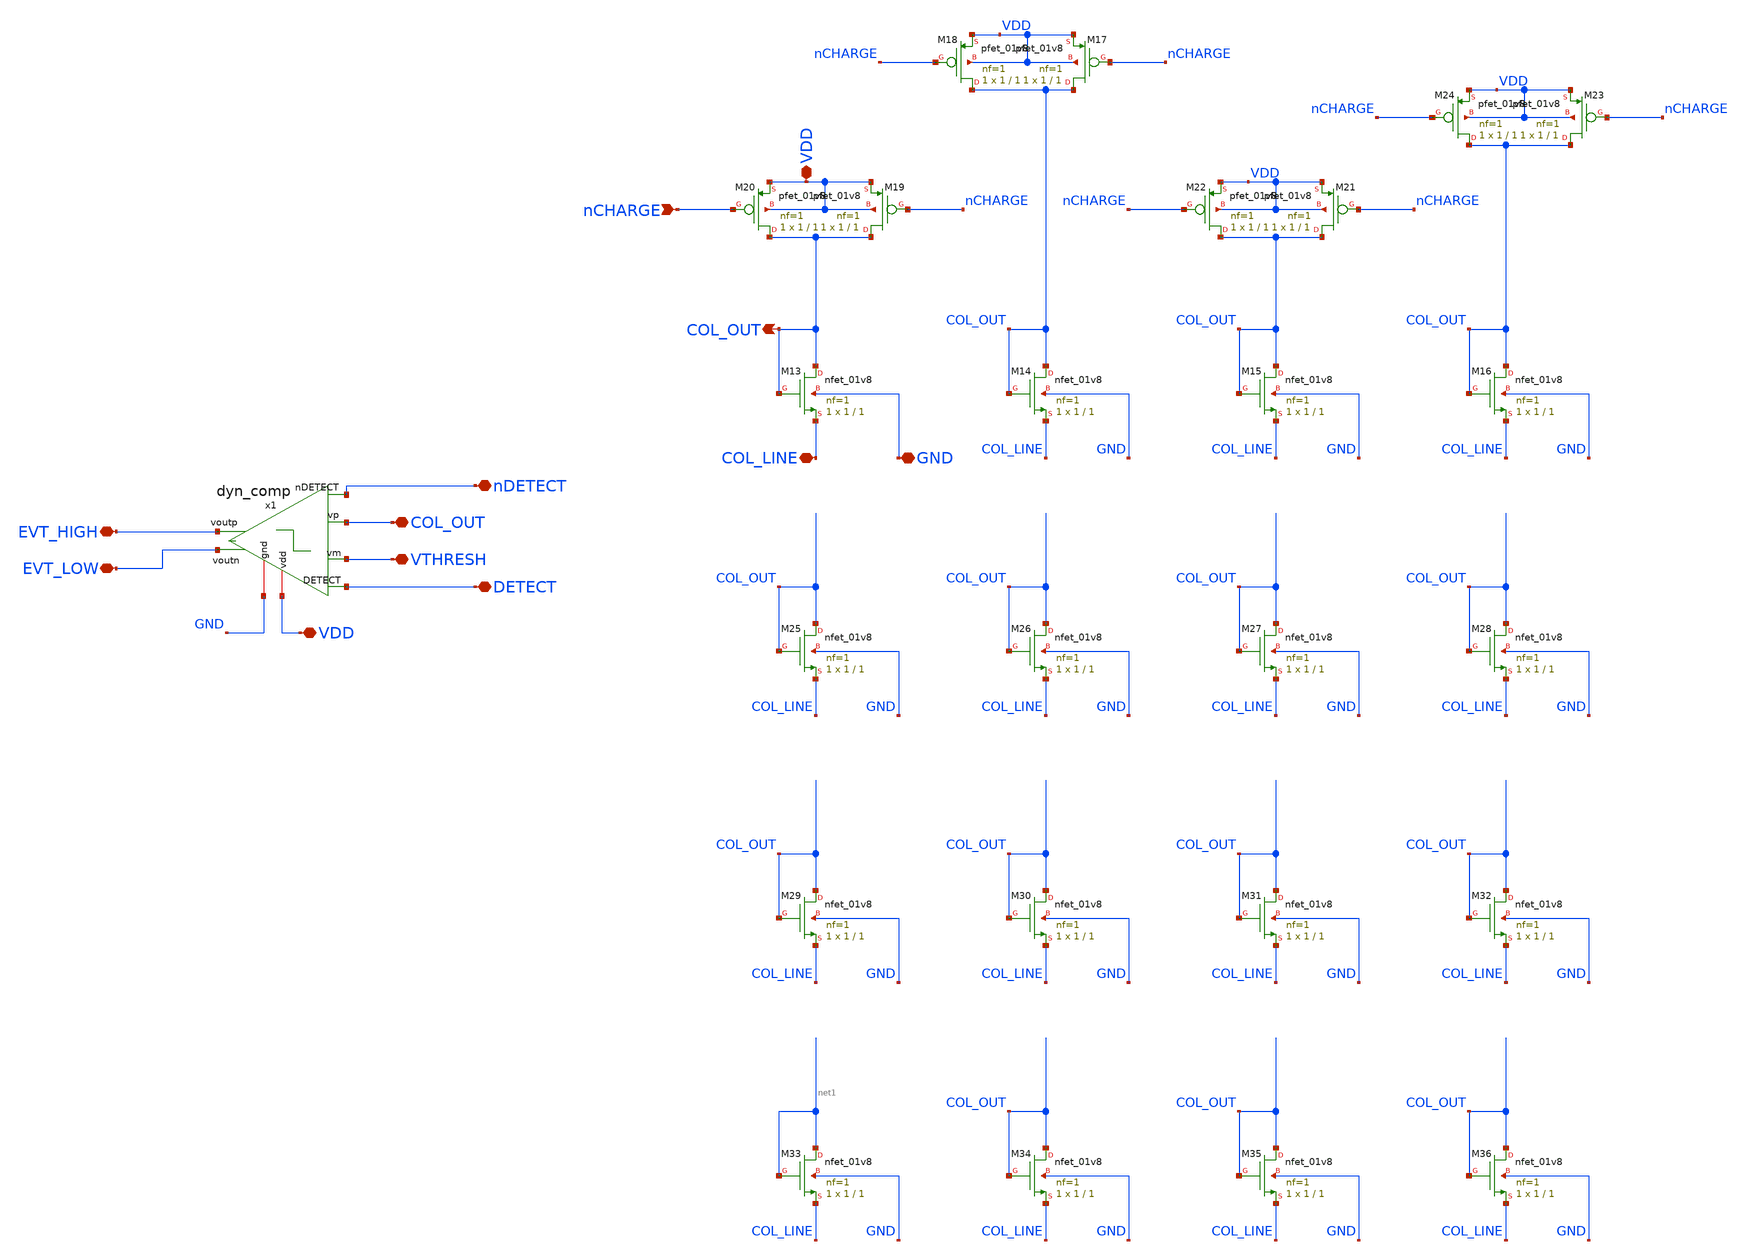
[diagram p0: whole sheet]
** sch_path: analog/xschem/col_amp_v2_std_vds/xschem/column_gds.sch
**.subckt column_gds DETECT VTHRESH VDD EVT_HIGH EVT_LOW nDETECT COL_OUT nCHARGE COL_OUT VDD GND
*+ COL_LINE
*.iopin DETECT
*.iopin VTHRESH
*.iopin VDD
*.iopin EVT_HIGH
*.iopin EVT_LOW
*.iopin nDETECT
*.iopin COL_OUT
*.ipin nCHARGE
*.opin COL_OUT
*.iopin VDD
*.iopin GND
*.iopin COL_LINE
XM13 COL_OUT COL_OUT COL_LINE GND sky130_fd_pr__nfet_01v8 L=1 W=1 nf=1 ad='int((1 + 1)/2) * 1 / 1 * 0.29'
+ as='int((1 + 2)/2) * 1 / 1 * 0.29' pd='2*int((1 + 1)/2) * (1 / 1 + 0.29)' ps='2*int((1 + 2)/2) * (1 / 1 + 0.29)'
+ nrd='0.29 / 1 ' nrs='0.29 / 1 ' sa=0 sb=0 sd=0 mult=1 m=1
XM14 COL_OUT COL_OUT COL_LINE GND sky130_fd_pr__nfet_01v8 L=1 W=1 nf=1 ad='int((1 + 1)/2) * 1 / 1 * 0.29'
+ as='int((1 + 2)/2) * 1 / 1 * 0.29' pd='2*int((1 + 1)/2) * (1 / 1 + 0.29)' ps='2*int((1 + 2)/2) * (1 / 1 + 0.29)'
+ nrd='0.29 / 1 ' nrs='0.29 / 1 ' sa=0 sb=0 sd=0 mult=1 m=1
XM15 COL_OUT COL_OUT COL_LINE GND sky130_fd_pr__nfet_01v8 L=1 W=1 nf=1 ad='int((1 + 1)/2) * 1 / 1 * 0.29'
+ as='int((1 + 2)/2) * 1 / 1 * 0.29' pd='2*int((1 + 1)/2) * (1 / 1 + 0.29)' ps='2*int((1 + 2)/2) * (1 / 1 + 0.29)'
+ nrd='0.29 / 1 ' nrs='0.29 / 1 ' sa=0 sb=0 sd=0 mult=1 m=1
XM16 COL_OUT COL_OUT COL_LINE GND sky130_fd_pr__nfet_01v8 L=1 W=1 nf=1 ad='int((1 + 1)/2) * 1 / 1 * 0.29'
+ as='int((1 + 2)/2) * 1 / 1 * 0.29' pd='2*int((1 + 1)/2) * (1 / 1 + 0.29)' ps='2*int((1 + 2)/2) * (1 / 1 + 0.29)'
+ nrd='0.29 / 1 ' nrs='0.29 / 1 ' sa=0 sb=0 sd=0 mult=1 m=1
XM17 COL_OUT nCHARGE VDD VDD sky130_fd_pr__pfet_01v8 L=1 W=1 nf=1 ad='int((1 + 1)/2) * 1 / 1 * 0.29'
+ as='int((1 + 2)/2) * 1 / 1 * 0.29' pd='2*int((1 + 1)/2) * (1 / 1 + 0.29)' ps='2*int((1 + 2)/2) * (1 / 1 + 0.29)'
+ nrd='0.29 / 1 ' nrs='0.29 / 1 ' sa=0 sb=0 sd=0 mult=1 m=1
XM18 COL_OUT nCHARGE VDD VDD sky130_fd_pr__pfet_01v8 L=1 W=1 nf=1 ad='int((1 + 1)/2) * 1 / 1 * 0.29'
+ as='int((1 + 2)/2) * 1 / 1 * 0.29' pd='2*int((1 + 1)/2) * (1 / 1 + 0.29)' ps='2*int((1 + 2)/2) * (1 / 1 + 0.29)'
+ nrd='0.29 / 1 ' nrs='0.29 / 1 ' sa=0 sb=0 sd=0 mult=1 m=1
XM19 COL_OUT nCHARGE VDD VDD sky130_fd_pr__pfet_01v8 L=1 W=1 nf=1 ad='int((1 + 1)/2) * 1 / 1 * 0.29'
+ as='int((1 + 2)/2) * 1 / 1 * 0.29' pd='2*int((1 + 1)/2) * (1 / 1 + 0.29)' ps='2*int((1 + 2)/2) * (1 / 1 + 0.29)'
+ nrd='0.29 / 1 ' nrs='0.29 / 1 ' sa=0 sb=0 sd=0 mult=1 m=1
XM20 COL_OUT nCHARGE VDD VDD sky130_fd_pr__pfet_01v8 L=1 W=1 nf=1 ad='int((1 + 1)/2) * 1 / 1 * 0.29'
+ as='int((1 + 2)/2) * 1 / 1 * 0.29' pd='2*int((1 + 1)/2) * (1 / 1 + 0.29)' ps='2*int((1 + 2)/2) * (1 / 1 + 0.29)'
+ nrd='0.29 / 1 ' nrs='0.29 / 1 ' sa=0 sb=0 sd=0 mult=1 m=1
XM21 COL_OUT nCHARGE VDD VDD sky130_fd_pr__pfet_01v8 L=1 W=1 nf=1 ad='int((1 + 1)/2) * 1 / 1 * 0.29'
+ as='int((1 + 2)/2) * 1 / 1 * 0.29' pd='2*int((1 + 1)/2) * (1 / 1 + 0.29)' ps='2*int((1 + 2)/2) * (1 / 1 + 0.29)'
+ nrd='0.29 / 1 ' nrs='0.29 / 1 ' sa=0 sb=0 sd=0 mult=1 m=1
XM22 COL_OUT nCHARGE VDD VDD sky130_fd_pr__pfet_01v8 L=1 W=1 nf=1 ad='int((1 + 1)/2) * 1 / 1 * 0.29'
+ as='int((1 + 2)/2) * 1 / 1 * 0.29' pd='2*int((1 + 1)/2) * (1 / 1 + 0.29)' ps='2*int((1 + 2)/2) * (1 / 1 + 0.29)'
+ nrd='0.29 / 1 ' nrs='0.29 / 1 ' sa=0 sb=0 sd=0 mult=1 m=1
XM23 COL_OUT nCHARGE VDD VDD sky130_fd_pr__pfet_01v8 L=1 W=1 nf=1 ad='int((1 + 1)/2) * 1 / 1 * 0.29'
+ as='int((1 + 2)/2) * 1 / 1 * 0.29' pd='2*int((1 + 1)/2) * (1 / 1 + 0.29)' ps='2*int((1 + 2)/2) * (1 / 1 + 0.29)'
+ nrd='0.29 / 1 ' nrs='0.29 / 1 ' sa=0 sb=0 sd=0 mult=1 m=1
XM24 COL_OUT nCHARGE VDD VDD sky130_fd_pr__pfet_01v8 L=1 W=1 nf=1 ad='int((1 + 1)/2) * 1 / 1 * 0.29'
+ as='int((1 + 2)/2) * 1 / 1 * 0.29' pd='2*int((1 + 1)/2) * (1 / 1 + 0.29)' ps='2*int((1 + 2)/2) * (1 / 1 + 0.29)'
+ nrd='0.29 / 1 ' nrs='0.29 / 1 ' sa=0 sb=0 sd=0 mult=1 m=1
XM25 COL_OUT COL_OUT COL_LINE GND sky130_fd_pr__nfet_01v8 L=1 W=1 nf=1 ad='int((1 + 1)/2) * 1 / 1 * 0.29'
+ as='int((1 + 2)/2) * 1 / 1 * 0.29' pd='2*int((1 + 1)/2) * (1 / 1 + 0.29)' ps='2*int((1 + 2)/2) * (1 / 1 + 0.29)'
+ nrd='0.29 / 1 ' nrs='0.29 / 1 ' sa=0 sb=0 sd=0 mult=1 m=1
XM26 COL_OUT COL_OUT COL_LINE GND sky130_fd_pr__nfet_01v8 L=1 W=1 nf=1 ad='int((1 + 1)/2) * 1 / 1 * 0.29'
+ as='int((1 + 2)/2) * 1 / 1 * 0.29' pd='2*int((1 + 1)/2) * (1 / 1 + 0.29)' ps='2*int((1 + 2)/2) * (1 / 1 + 0.29)'
+ nrd='0.29 / 1 ' nrs='0.29 / 1 ' sa=0 sb=0 sd=0 mult=1 m=1
XM27 COL_OUT COL_OUT COL_LINE GND sky130_fd_pr__nfet_01v8 L=1 W=1 nf=1 ad='int((1 + 1)/2) * 1 / 1 * 0.29'
+ as='int((1 + 2)/2) * 1 / 1 * 0.29' pd='2*int((1 + 1)/2) * (1 / 1 + 0.29)' ps='2*int((1 + 2)/2) * (1 / 1 + 0.29)'
+ nrd='0.29 / 1 ' nrs='0.29 / 1 ' sa=0 sb=0 sd=0 mult=1 m=1
XM28 COL_OUT COL_OUT COL_LINE GND sky130_fd_pr__nfet_01v8 L=1 W=1 nf=1 ad='int((1 + 1)/2) * 1 / 1 * 0.29'
+ as='int((1 + 2)/2) * 1 / 1 * 0.29' pd='2*int((1 + 1)/2) * (1 / 1 + 0.29)' ps='2*int((1 + 2)/2) * (1 / 1 + 0.29)'
+ nrd='0.29 / 1 ' nrs='0.29 / 1 ' sa=0 sb=0 sd=0 mult=1 m=1
XM29 COL_OUT COL_OUT COL_LINE GND sky130_fd_pr__nfet_01v8 L=1 W=1 nf=1 ad='int((1 + 1)/2) * 1 / 1 * 0.29'
+ as='int((1 + 2)/2) * 1 / 1 * 0.29' pd='2*int((1 + 1)/2) * (1 / 1 + 0.29)' ps='2*int((1 + 2)/2) * (1 / 1 + 0.29)'
+ nrd='0.29 / 1 ' nrs='0.29 / 1 ' sa=0 sb=0 sd=0 mult=1 m=1
XM30 COL_OUT COL_OUT COL_LINE GND sky130_fd_pr__nfet_01v8 L=1 W=1 nf=1 ad='int((1 + 1)/2) * 1 / 1 * 0.29'
+ as='int((1 + 2)/2) * 1 / 1 * 0.29' pd='2*int((1 + 1)/2) * (1 / 1 + 0.29)' ps='2*int((1 + 2)/2) * (1 / 1 + 0.29)'
+ nrd='0.29 / 1 ' nrs='0.29 / 1 ' sa=0 sb=0 sd=0 mult=1 m=1
XM31 COL_OUT COL_OUT COL_LINE GND sky130_fd_pr__nfet_01v8 L=1 W=1 nf=1 ad='int((1 + 1)/2) * 1 / 1 * 0.29'
+ as='int((1 + 2)/2) * 1 / 1 * 0.29' pd='2*int((1 + 1)/2) * (1 / 1 + 0.29)' ps='2*int((1 + 2)/2) * (1 / 1 + 0.29)'
+ nrd='0.29 / 1 ' nrs='0.29 / 1 ' sa=0 sb=0 sd=0 mult=1 m=1
XM32 COL_OUT COL_OUT COL_LINE GND sky130_fd_pr__nfet_01v8 L=1 W=1 nf=1 ad='int((1 + 1)/2) * 1 / 1 * 0.29'
+ as='int((1 + 2)/2) * 1 / 1 * 0.29' pd='2*int((1 + 1)/2) * (1 / 1 + 0.29)' ps='2*int((1 + 2)/2) * (1 / 1 + 0.29)'
+ nrd='0.29 / 1 ' nrs='0.29 / 1 ' sa=0 sb=0 sd=0 mult=1 m=1
XM33 net1 net1 COL_LINE GND sky130_fd_pr__nfet_01v8 L=1 W=1 nf=1 ad='int((1 + 1)/2) * 1 / 1 * 0.29' as='int((1 + 2)/2) * 1 / 1 * 0.29'
+ pd='2*int((1 + 1)/2) * (1 / 1 + 0.29)' ps='2*int((1 + 2)/2) * (1 / 1 + 0.29)' nrd='0.29 / 1 ' nrs='0.29 / 1 '
+ sa=0 sb=0 sd=0 mult=1 m=1
XM34 COL_OUT COL_OUT COL_LINE GND sky130_fd_pr__nfet_01v8 L=1 W=1 nf=1 ad='int((1 + 1)/2) * 1 / 1 * 0.29'
+ as='int((1 + 2)/2) * 1 / 1 * 0.29' pd='2*int((1 + 1)/2) * (1 / 1 + 0.29)' ps='2*int((1 + 2)/2) * (1 / 1 + 0.29)'
+ nrd='0.29 / 1 ' nrs='0.29 / 1 ' sa=0 sb=0 sd=0 mult=1 m=1
XM35 COL_OUT COL_OUT COL_LINE GND sky130_fd_pr__nfet_01v8 L=1 W=1 nf=1 ad='int((1 + 1)/2) * 1 / 1 * 0.29'
+ as='int((1 + 2)/2) * 1 / 1 * 0.29' pd='2*int((1 + 1)/2) * (1 / 1 + 0.29)' ps='2*int((1 + 2)/2) * (1 / 1 + 0.29)'
+ nrd='0.29 / 1 ' nrs='0.29 / 1 ' sa=0 sb=0 sd=0 mult=1 m=1
XM36 COL_OUT COL_OUT COL_LINE GND sky130_fd_pr__nfet_01v8 L=1 W=1 nf=1 ad='int((1 + 1)/2) * 1 / 1 * 0.29'
+ as='int((1 + 2)/2) * 1 / 1 * 0.29' pd='2*int((1 + 1)/2) * (1 / 1 + 0.29)' ps='2*int((1 + 2)/2) * (1 / 1 + 0.29)'
+ nrd='0.29 / 1 ' nrs='0.29 / 1 ' sa=0 sb=0 sd=0 mult=1 m=1
x1 VDD COL_OUT VTHRESH GND nDETECT DETECT EVT_HIGH EVT_LOW dyn_comp
**.ends

* expanding   symbol:  dyn_comp.sym # of pins=8
** sym_path: analog/xschem/col_amp_v2_std_dvs/xschem/dyn_comp.sym
** sch_path: analog/xschem/col_amp_v2_std_dvs/xschem/dyn_comp.sch
.subckt dyn_comp vdd vp vm gnd nDETECT DETECT voutp voutn
*.iopin vdd
*.iopin gnd
*.ipin vp
*.ipin vm
*.ipin nDETECT
*.opin voutn
*.opin voutp
*.ipin DETECT
XMmirr3 int_outn DETECT vdd vdd sky130_fd_pr__pfet_01v8 L=0.5 W=1 nf=1 ad='int((1 + 1)/2) * 1 / 1 * 0.29'
+ as='int((1 + 2)/2) * 1 / 1 * 0.29' pd='2*int((1 + 1)/2) * (1 / 1 + 0.29)' ps='2*int((1 + 2)/2) * (1 / 1 + 0.29)'
+ nrd='0.29 / 1 ' nrs='0.29 / 1 ' sa=0 sb=0 sd=0 mult=1 m=1
XMdio2 int_outp DETECT vdd vdd sky130_fd_pr__pfet_01v8 L=0.5 W=1 nf=1 ad='int((1 + 1)/2) * 1 / 1 * 0.29'
+ as='int((1 + 2)/2) * 1 / 1 * 0.29' pd='2*int((1 + 1)/2) * (1 / 1 + 0.29)' ps='2*int((1 + 2)/2) * (1 / 1 + 0.29)'
+ nrd='0.29 / 1 ' nrs='0.29 / 1 ' sa=0 sb=0 sd=0 mult=1 m=1
XMinm3 int_outp vp vsource gnd sky130_fd_pr__nfet_01v8 L=0.15 W=1 nf=1 ad='int((1 + 1)/2) * 1 / 1 * 0.29'
+ as='int((1 + 2)/2) * 1 / 1 * 0.29' pd='2*int((1 + 1)/2) * (1 / 1 + 0.29)' ps='2*int((1 + 2)/2) * (1 / 1 + 0.29)'
+ nrd='0.29 / 1 ' nrs='0.29 / 1 ' sa=0 sb=0 sd=0 mult=1 m=1
XMinp3 int_outn vm vsource gnd sky130_fd_pr__nfet_01v8 L=0.15 W=1 nf=1 ad='int((1 + 1)/2) * 1 / 1 * 0.29'
+ as='int((1 + 2)/2) * 1 / 1 * 0.29' pd='2*int((1 + 1)/2) * (1 / 1 + 0.29)' ps='2*int((1 + 2)/2) * (1 / 1 + 0.29)'
+ nrd='0.29 / 1 ' nrs='0.29 / 1 ' sa=0 sb=0 sd=0 mult=1 m=1
XMbias1 vsource DETECT gnd gnd sky130_fd_pr__nfet_01v8 L=0.15 W=1 nf=1 ad='int((1 + 1)/2) * 1 / 1 * 0.29'
+ as='int((1 + 2)/2) * 1 / 1 * 0.29' pd='2*int((1 + 1)/2) * (1 / 1 + 0.29)' ps='2*int((1 + 2)/2) * (1 / 1 + 0.29)'
+ nrd='0.29 / 1 ' nrs='0.29 / 1 ' sa=0 sb=0 sd=0 mult=1 m=1
XMmirr4 net3 nDETECT vdd vdd sky130_fd_pr__pfet_01v8 L=0.5 W=1 nf=1 ad='int((1 + 1)/2) * 1 / 1 * 0.29'
+ as='int((1 + 2)/2) * 1 / 1 * 0.29' pd='2*int((1 + 1)/2) * (1 / 1 + 0.29)' ps='2*int((1 + 2)/2) * (1 / 1 + 0.29)'
+ nrd='0.29 / 1 ' nrs='0.29 / 1 ' sa=0 sb=0 sd=0 mult=1 m=1
XMmirr5 net2 net1 net3 vdd sky130_fd_pr__pfet_01v8 L=0.5 W=1 nf=1 ad='int((1 + 1)/2) * 1 / 1 * 0.29'
+ as='int((1 + 2)/2) * 1 / 1 * 0.29' pd='2*int((1 + 1)/2) * (1 / 1 + 0.29)' ps='2*int((1 + 2)/2) * (1 / 1 + 0.29)'
+ nrd='0.29 / 1 ' nrs='0.29 / 1 ' sa=0 sb=0 sd=0 mult=1 m=1
XMdio3 net1 net2 net3 vdd sky130_fd_pr__pfet_01v8 L=0.5 W=1 nf=1 ad='int((1 + 1)/2) * 1 / 1 * 0.29' as='int((1 + 2)/2) * 1 / 1 * 0.29'
+ pd='2*int((1 + 1)/2) * (1 / 1 + 0.29)' ps='2*int((1 + 2)/2) * (1 / 1 + 0.29)' nrd='0.29 / 1 ' nrs='0.29 / 1 '
+ sa=0 sb=0 sd=0 mult=1 m=1
XMinp4 net1 net2 gnd gnd sky130_fd_pr__nfet_01v8 L=0.15 W=1 nf=1 ad='int((1 + 1)/2) * 1 / 1 * 0.29' as='int((1 + 2)/2) * 1 / 1 * 0.29'
+ pd='2*int((1 + 1)/2) * (1 / 1 + 0.29)' ps='2*int((1 + 2)/2) * (1 / 1 + 0.29)' nrd='0.29 / 1 ' nrs='0.29 / 1 '
+ sa=0 sb=0 sd=0 mult=1 m=1
XMinm4 net2 net1 gnd gnd sky130_fd_pr__nfet_01v8 L=0.15 W=1 nf=1 ad='int((1 + 1)/2) * 1 / 1 * 0.29' as='int((1 + 2)/2) * 1 / 1 * 0.29'
+ pd='2*int((1 + 1)/2) * (1 / 1 + 0.29)' ps='2*int((1 + 2)/2) * (1 / 1 + 0.29)' nrd='0.29 / 1 ' nrs='0.29 / 1 '
+ sa=0 sb=0 sd=0 mult=1 m=1
XMinm5 net1 int_outp gnd gnd sky130_fd_pr__nfet_01v8 L=0.15 W=1 nf=1 ad='int((1 + 1)/2) * 1 / 1 * 0.29'
+ as='int((1 + 2)/2) * 1 / 1 * 0.29' pd='2*int((1 + 1)/2) * (1 / 1 + 0.29)' ps='2*int((1 + 2)/2) * (1 / 1 + 0.29)'
+ nrd='0.29 / 1 ' nrs='0.29 / 1 ' sa=0 sb=0 sd=0 mult=4 m=4
XMinp5 net2 int_outn gnd gnd sky130_fd_pr__nfet_01v8 L=0.15 W=1 nf=1 ad='int((1 + 1)/2) * 1 / 1 * 0.29'
+ as='int((1 + 2)/2) * 1 / 1 * 0.29' pd='2*int((1 + 1)/2) * (1 / 1 + 0.29)' ps='2*int((1 + 2)/2) * (1 / 1 + 0.29)'
+ nrd='0.29 / 1 ' nrs='0.29 / 1 ' sa=0 sb=0 sd=0 mult=4 m=4
XMmirr1 voutp net2 vdd vdd sky130_fd_pr__pfet_01v8 L=1 W=2 nf=1 ad='int((1 + 1)/2) * 2 / 1 * 0.29' as='int((1 + 2)/2) * 2 / 1 * 0.29'
+ pd='2*int((1 + 1)/2) * (2 / 1 + 0.29)' ps='2*int((1 + 2)/2) * (2 / 1 + 0.29)' nrd='0.29 / 2 ' nrs='0.29 / 2 '
+ sa=0 sb=0 sd=0 mult=1 m=1
XMinm1 voutp net2 gnd gnd sky130_fd_pr__nfet_01v8 L=1 W=1 nf=1 ad='int((1 + 1)/2) * 1 / 1 * 0.29' as='int((1 + 2)/2) * 1 / 1 * 0.29'
+ pd='2*int((1 + 1)/2) * (1 / 1 + 0.29)' ps='2*int((1 + 2)/2) * (1 / 1 + 0.29)' nrd='0.29 / 1 ' nrs='0.29 / 1 '
+ sa=0 sb=0 sd=0 mult=1 m=1
XMmirr2 voutn net1 vdd vdd sky130_fd_pr__pfet_01v8 L=1 W=2 nf=1 ad='int((1 + 1)/2) * 2 / 1 * 0.29' as='int((1 + 2)/2) * 2 / 1 * 0.29'
+ pd='2*int((1 + 1)/2) * (2 / 1 + 0.29)' ps='2*int((1 + 2)/2) * (2 / 1 + 0.29)' nrd='0.29 / 2 ' nrs='0.29 / 2 '
+ sa=0 sb=0 sd=0 mult=1 m=1
XMinm2 voutn net1 gnd gnd sky130_fd_pr__nfet_01v8 L=1 W=1 nf=1 ad='int((1 + 1)/2) * 1 / 1 * 0.29' as='int((1 + 2)/2) * 1 / 1 * 0.29'
+ pd='2*int((1 + 1)/2) * (1 / 1 + 0.29)' ps='2*int((1 + 2)/2) * (1 / 1 + 0.29)' nrd='0.29 / 1 ' nrs='0.29 / 1 '
+ sa=0 sb=0 sd=0 mult=1 m=1
.ends

.end
